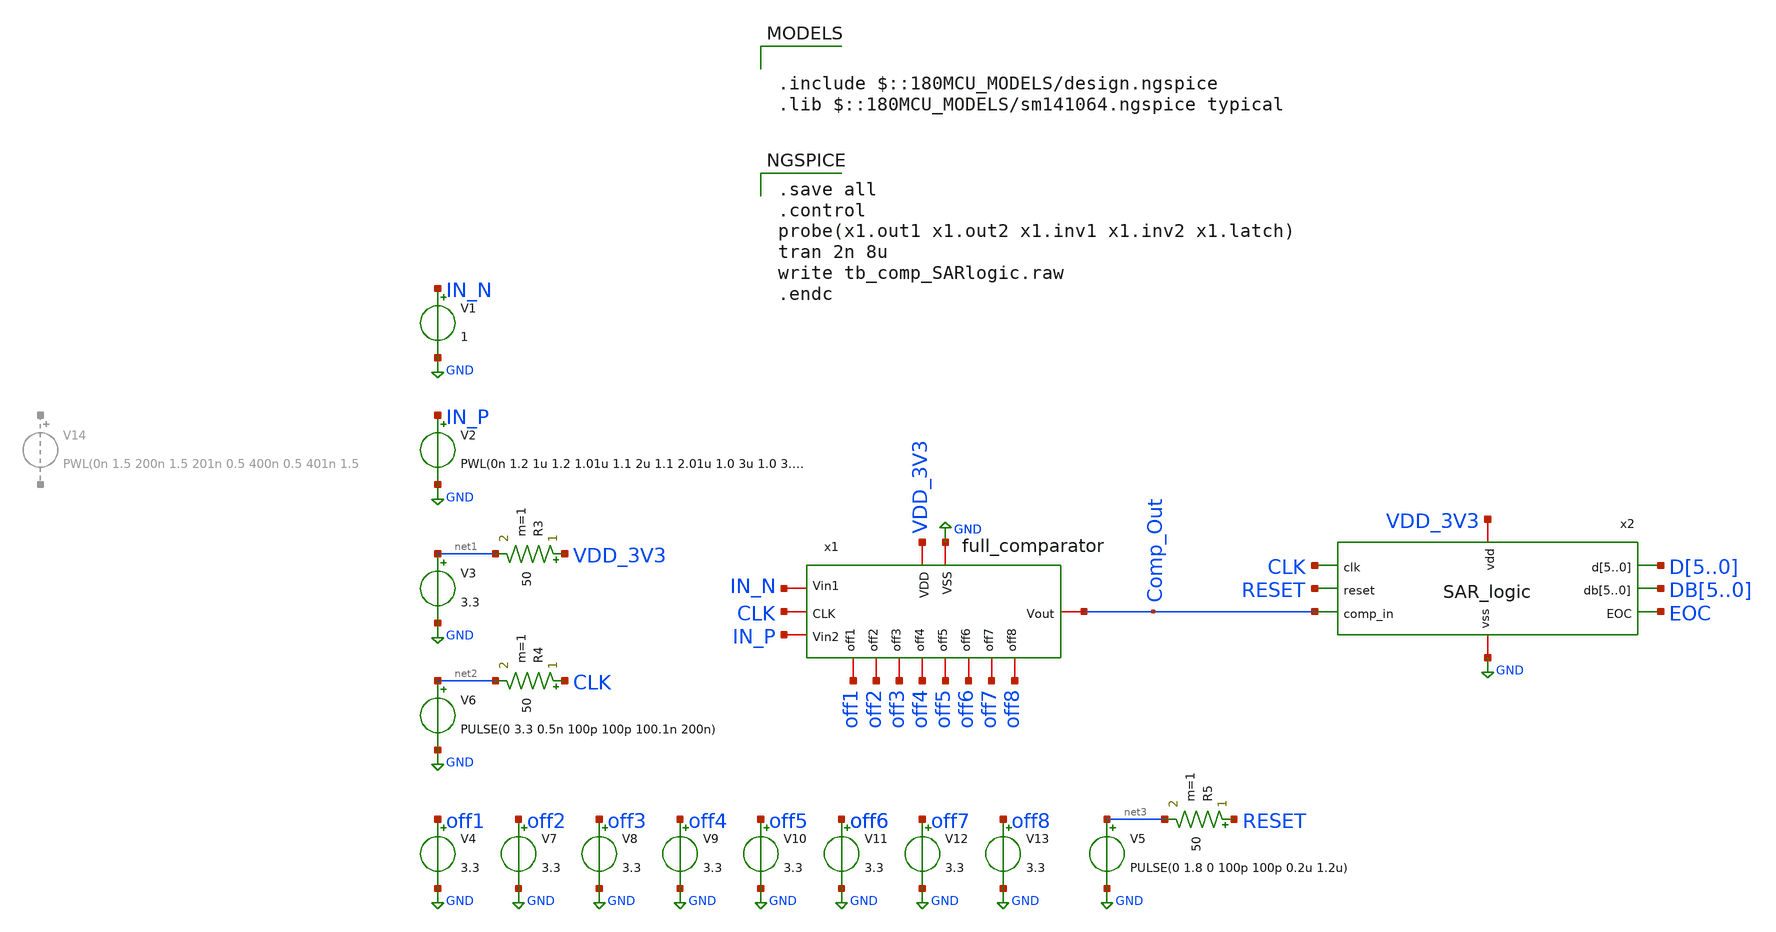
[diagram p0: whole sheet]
** sch_path: designs/full_ADC/tb_comp_SARlogic_mk_test.sch
**.subckt tb_comp_SARlogic_mk_test
x1 off1 VDD_3V3 GND off2 CLK off3 IN_N off4 IN_P off5 Comp_Out off6 off7 off8 full_comparator
V4 off1 GND 3.3
V7 off2 GND 3.3
V8 off3 GND 3.3
V9 off4 GND 3.3
V10 off5 GND 3.3
V11 off6 GND 3.3
V12 off7 GND 3.3
V13 off8 GND 3.3
V3 net1 GND 3.3
V6 net2 GND PULSE(0 3.3 0.5n 100p 100p 100.1n 200n)
R3 VDD_3V3 net1 50 m=1
R4 CLK net2 50 m=1
V2 IN_P GND PWL(0n 1.2 1u 1.2 1.01u 1.1 2u 1.1 2.01u 1.0 3u 1.0 3.01u 0.95 4u 0.95 4.01u 0.9 5u 1.1
+ 5.01u 1.1
V1 IN_N GND 1
x2 VDD_3V3 GND CLK RESET Comp_Out D5 D4 D3 D2 D1 D0 DB5 DB4 DB3 DB2 DB1 DB0 EOC SAR_logic
V5 net3 GND PULSE(0 1.8 0 100p 100p 0.2u 1.2u)
R5 RESET net3 50 m=1
**** begin user architecture code

.include $::180MCU_MODELS/design.ngspice
.lib $::180MCU_MODELS/sm141064.ngspice typical


.save all
.control
probe(x1.out1 x1.out2 x1.inv1 x1.inv2 x1.latch)
tran 2n 8u
write tb_comp_SARlogic.raw
.endc

**** end user architecture code
**.ends
.GLOBAL GND
.end
